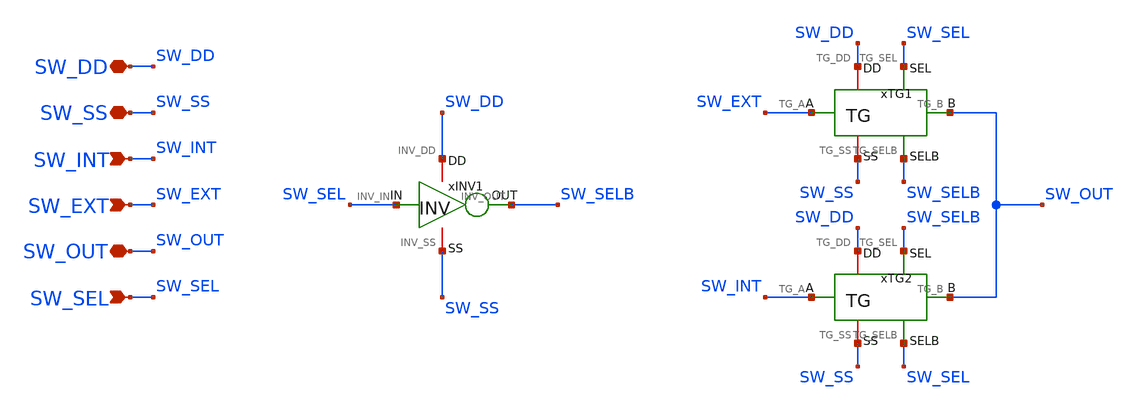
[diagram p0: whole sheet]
** sch_path: Design_Files/IC Design/Schematic/AFE_BLOCKS/SW/SW.sch
**.subckt SW SW_DD SW_SS SW_INT SW_OUT SW_EXT SW_SEL
*.iopin SW_DD
*.iopin SW_SS
*.ipin SW_INT
*.iopin SW_OUT
*.ipin SW_EXT
*.ipin SW_SEL
xINV1 SW_DD SW_SS SW_SEL SW_SELB INV
xTG1 SW_DD SW_SS SW_EXT SW_OUT SW_SEL SW_SELB TG
xTG2 SW_DD SW_SS SW_INT SW_OUT SW_SELB SW_SEL TG
**.ends

* expanding   symbol:  ECG_Acquisition_IC/Design_Files/IC Design/Schematic/AFE_BLOCKS/INV/INV.sym #
*+ of pins=4
** sym_path: Design_Files/IC Design/Schematic/INV/INV.sym
** sch_path: Design_Files/IC Design/Schematic/INV/INV.sch
.subckt INV INV_DD INV_SS INV_IN INV_OUT
*.iopin INV_DD
*.iopin INV_SS
*.ipin INV_IN
*.opin INV_OUT
XMINVP INV_OUT INV_IN INV_DD INV_DD pfet_03v3 L=0.5u W=2u nf=1 ad='int((nf+1)/2) * W/nf * 0.18u' as='int((nf+2)/2) * W/nf * 0.18u'
+ pd='2*int((nf+1)/2) * (W/nf + 0.18u)' ps='2*int((nf+2)/2) * (W/nf + 0.18u)' nrd='0.18u / W' nrs='0.18u / W'
+ sa=0 sb=0 sd=0 m=1
XMINVN INV_OUT INV_IN INV_SS INV_SS nfet_03v3 L=0.5u W=1u nf=1 ad='int((nf+1)/2) * W/nf * 0.18u' as='int((nf+2)/2) * W/nf * 0.18u'
+ pd='2*int((nf+1)/2) * (W/nf + 0.18u)' ps='2*int((nf+2)/2) * (W/nf + 0.18u)' nrd='0.18u / W' nrs='0.18u / W'
+ sa=0 sb=0 sd=0 m=1
.ends


* expanding   symbol:  ECG_Acquisition_IC/Design_Files/IC Design/Schematic/AFE_BLOCKS/TG/TG.sym # of
*+ pins=6
** sym_path: Design_Files/IC Design/Schematic/TG/TG.sym
** sch_path: Design_Files/IC Design/Schematic/TG/TG.sch
.subckt TG TG_DD TG_SS TG_A TG_B TG_SEL TG_SELB
*.iopin TG_DD
*.iopin TG_SS
*.iopin TG_A
*.iopin TG_B
*.ipin TG_SEL
*.ipin TG_SELB
XMTGP TG_B TG_SELB TG_A TG_DD pfet_03v3 L=0.5u W=40u nf=1 ad='int((nf+1)/2) * W/nf * 0.18u' as='int((nf+2)/2) * W/nf * 0.18u'
+ pd='2*int((nf+1)/2) * (W/nf + 0.18u)' ps='2*int((nf+2)/2) * (W/nf + 0.18u)' nrd='0.18u / W' nrs='0.18u / W'
+ sa=0 sb=0 sd=0 m=1
XMTGN TG_A TG_SEL TG_B TG_SS nfet_03v3 L=0.5u W=20u nf=1 ad='int((nf+1)/2) * W/nf * 0.18u' as='int((nf+2)/2) * W/nf * 0.18u'
+ pd='2*int((nf+1)/2) * (W/nf + 0.18u)' ps='2*int((nf+2)/2) * (W/nf + 0.18u)' nrd='0.18u / W' nrs='0.18u / W'
+ sa=0 sb=0 sd=0 m=1
.ends

.end
